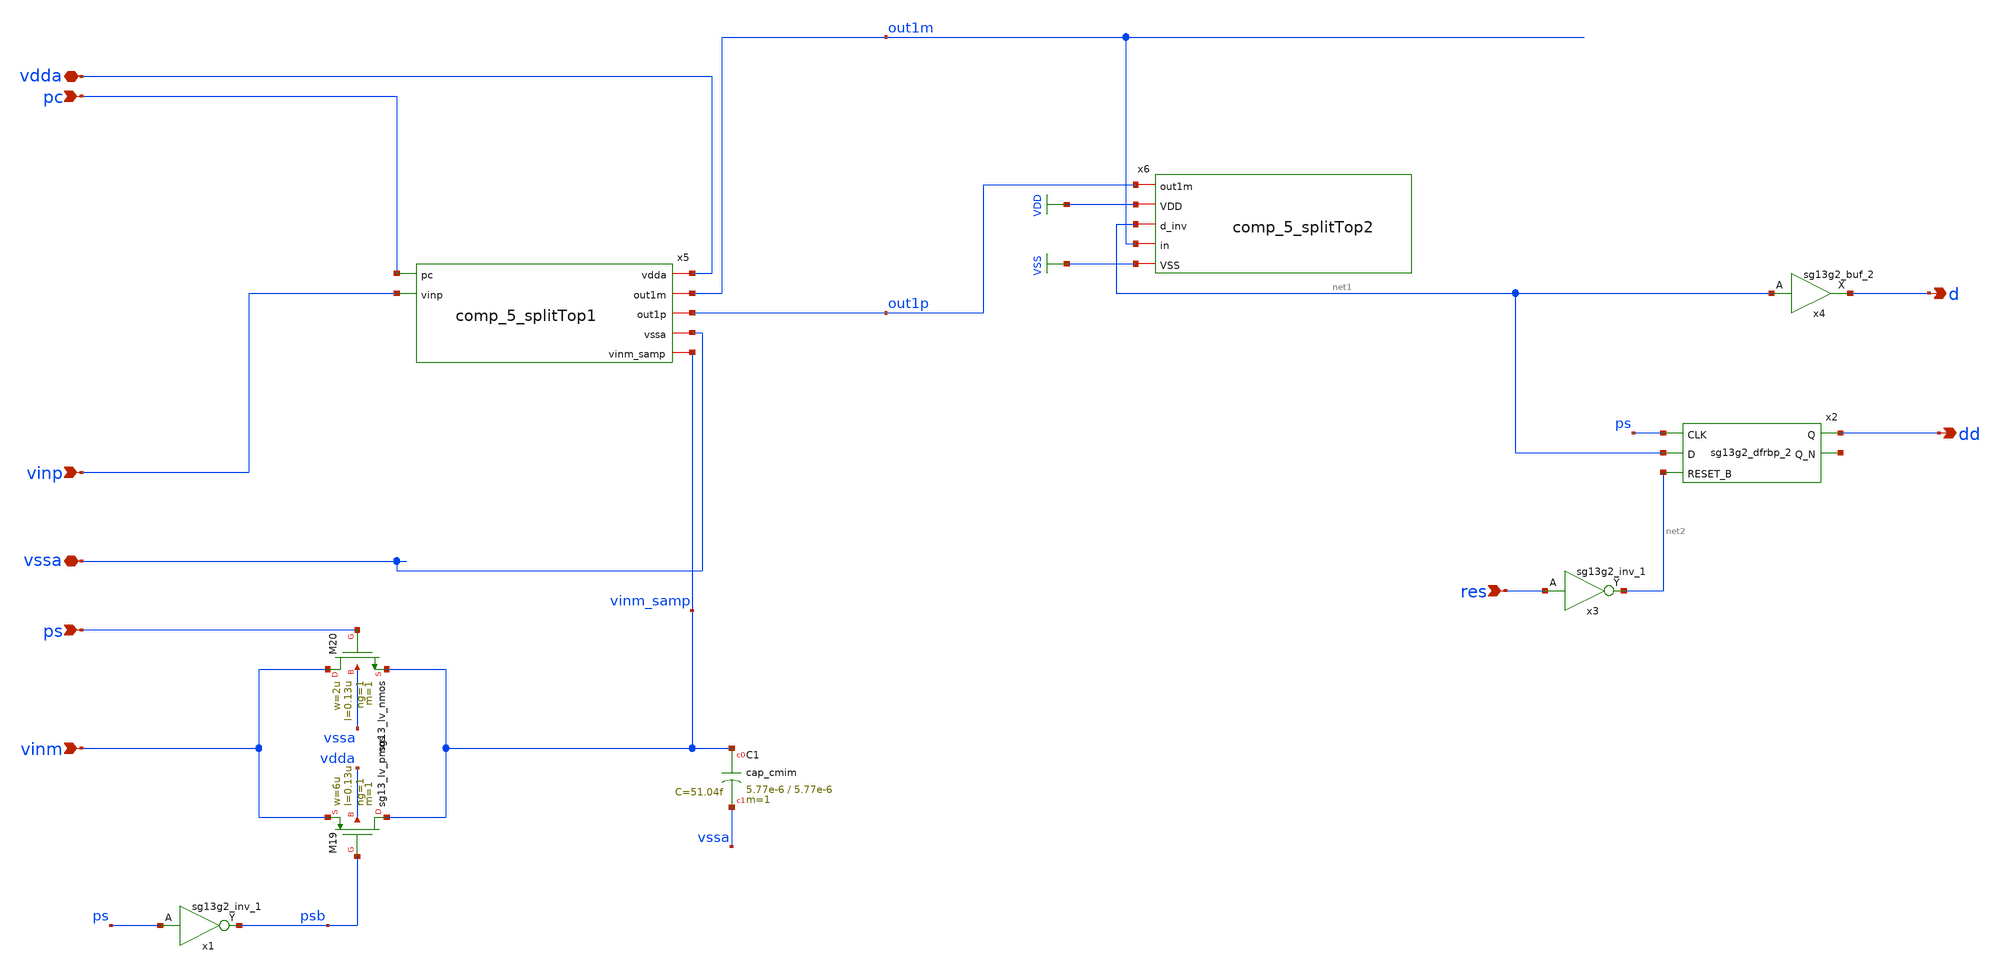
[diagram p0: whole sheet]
** sch_path: 5_Design/4_Layout/Team 5/splitUpSimulationsAndSchematics/comp_5_splitTop_test.sch
**.subckt comp_5_splitTop_test pc vdda vssa vinp ps vinm res dd d
*.ipin pc
*.iopin vdda
*.iopin vssa
*.ipin vinp
*.ipin ps
*.ipin vinm
*.ipin res
*.opin dd
*.opin d
XM19 vinm_samp psb vinm vdda sg13_lv_pmos w=6u l=0.13u ng=1 m=1 mm_ok=1
XM20 vinm ps vinm_samp vssa sg13_lv_nmos w=2u l=0.13u ng=1 m=1 mm_ok=1
x1 psb ps VDD VSS sg13g2_inv_1
XC1 vinm_samp vssa cap_cmim w=5.77e-6 l=5.77e-6 m=1 mm_ok=1
x2 dd net3 ps net1 net2 VDD VSS sg13g2_dfrbp_2
x3 net2 res VDD VSS sg13g2_inv_1
x4 d net1 VDD VSS sg13g2_buf_2
x5 vdda pc vinp out1m out1p vssa vinm_samp comp_5_splitTop1
x6 out1p VDD net1 out1m VSS comp_5_splitTop2
**.ends
.GLOBAL VDD
.GLOBAL VSS
.end
